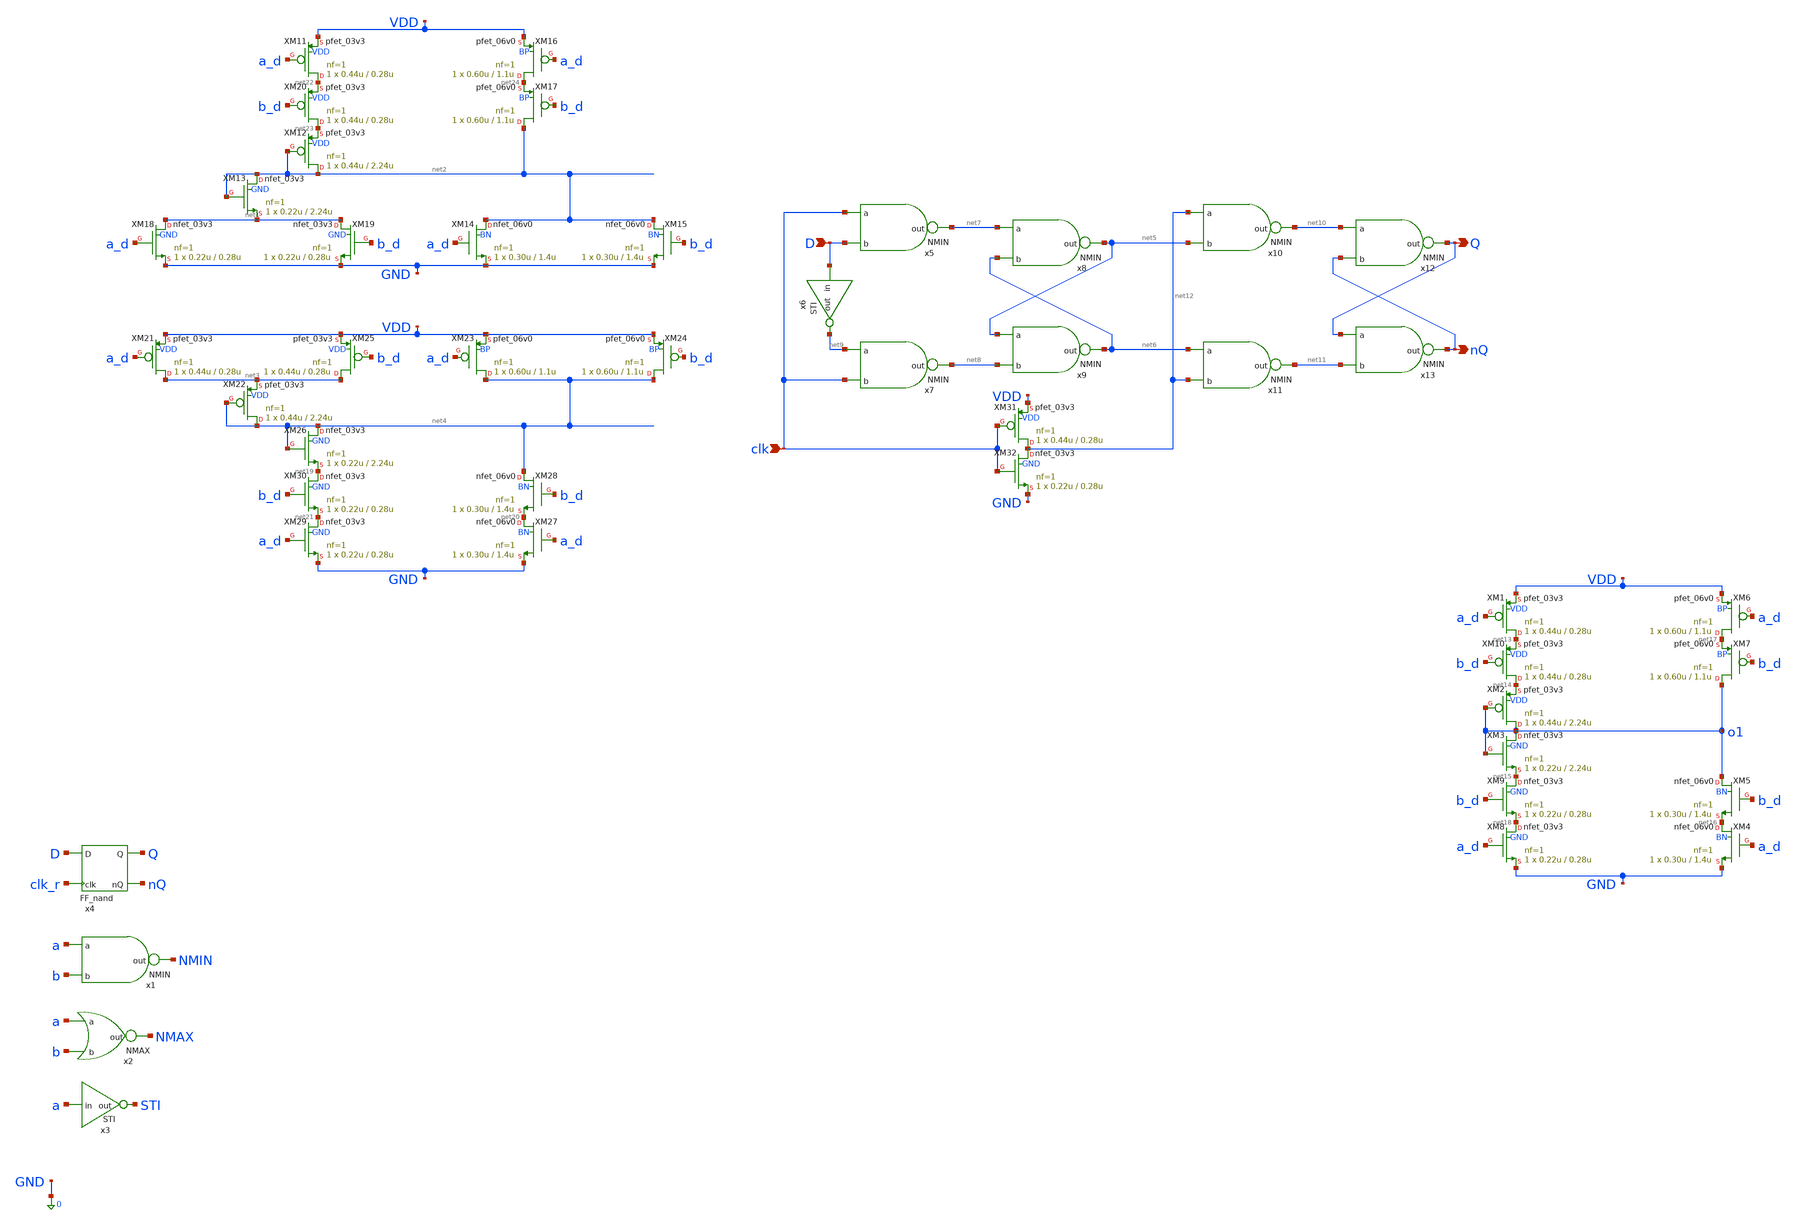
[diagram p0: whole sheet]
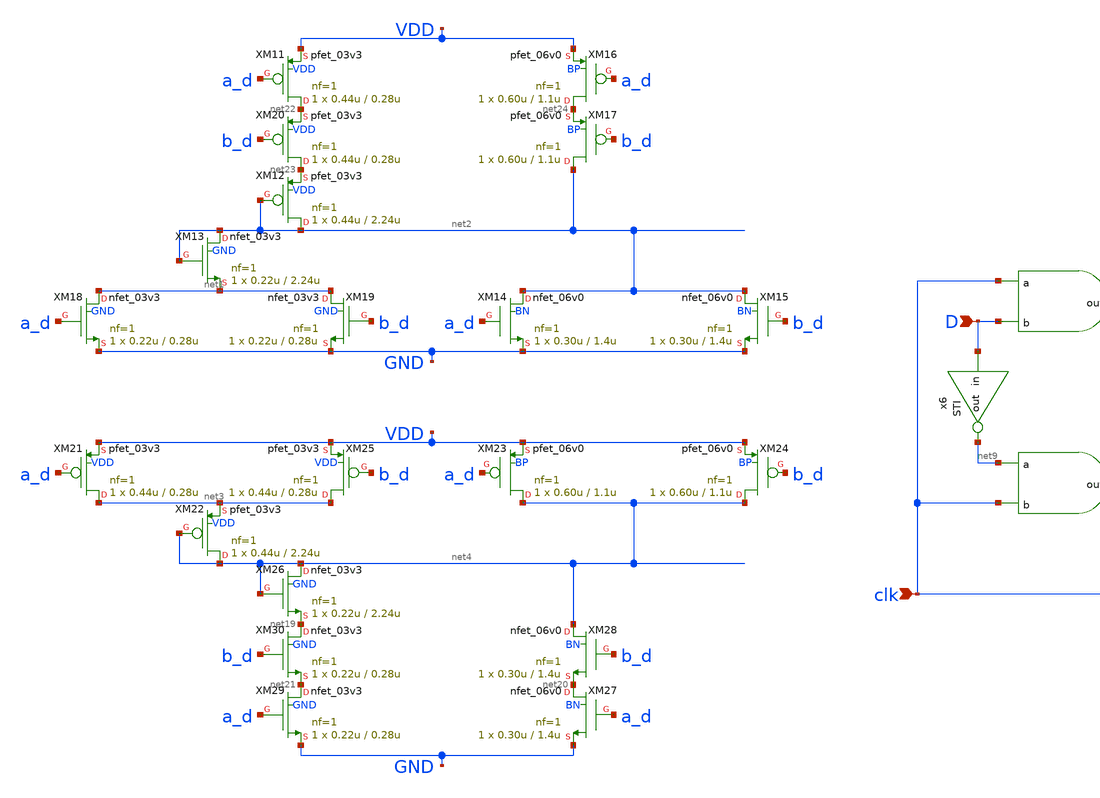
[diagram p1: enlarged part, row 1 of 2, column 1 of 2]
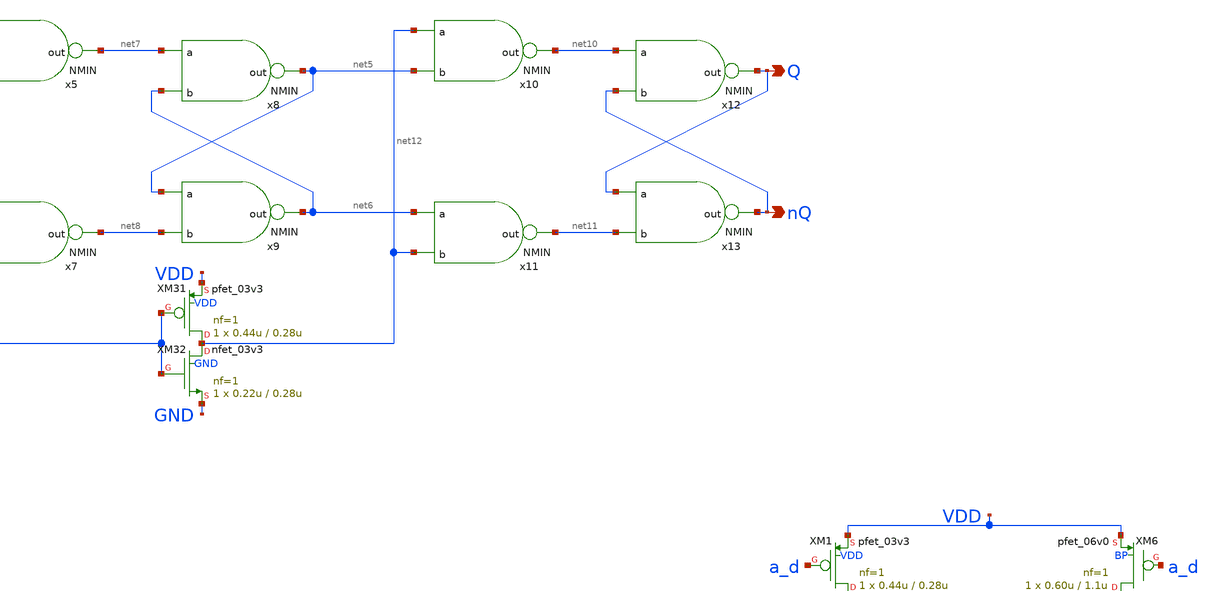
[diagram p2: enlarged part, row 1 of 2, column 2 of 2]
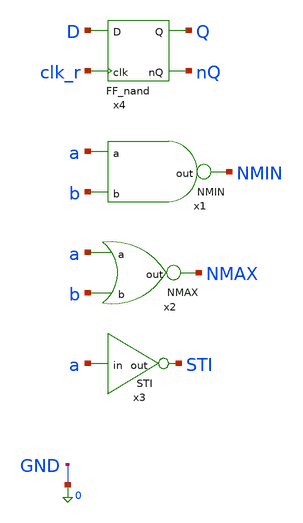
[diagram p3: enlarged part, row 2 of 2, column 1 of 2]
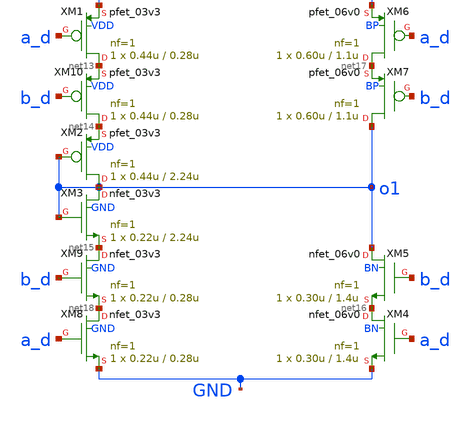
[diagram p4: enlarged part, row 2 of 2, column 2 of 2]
** sch_path: xschem_designs/NMIN_TB.sch
**.subckt NMIN_TB D clk Q nQ
*.ipin D
*.ipin clk
*.opin Q
*.opin nQ
x1 NMIN a b NMIN
XM1 net13 a_d VDD VDD pfet_03v3 L=0.28u W=0.44u nf=1 ad='int((nf+1)/2) * W/nf * 0.18u' as='int((nf+2)/2) * W/nf * 0.18u'
+ pd='2*int((nf+1)/2) * (W/nf + 0.18u)' ps='2*int((nf+2)/2) * (W/nf + 0.18u)' nrd='0.18u / W' nrs='0.18u / W'
+ sa=0 sb=0 sd=0 m=1 par=1
XM2 o1 o1 net14 VDD pfet_03v3 L=2.24u W=0.44u nf=1 ad='int((nf+1)/2) * W/nf * 0.18u' as='int((nf+2)/2) * W/nf * 0.18u'
+ pd='2*int((nf+1)/2) * (W/nf + 0.18u)' ps='2*int((nf+2)/2) * (W/nf + 0.18u)' nrd='0.18u / W' nrs='0.18u / W'
+ sa=0 sb=0 sd=0 m=1 par=1
XM3 o1 o1 net15 GND nfet_03v3 L=2.24u W=0.22u nf=1 ad='int((nf+1)/2) * W/nf * 0.18u' as='int((nf+2)/2) * W/nf * 0.18u'
+ pd='2*int((nf+1)/2) * (W/nf + 0.18u)' ps='2*int((nf+2)/2) * (W/nf + 0.18u)' nrd='0.18u / W' nrs='0.18u / W'
+ sa=0 sb=0 sd=0 m=1 par=1
XM4 net16 a_d GND BN nfet_06v0 L=1.4u W=0.30u nf=1 ad='int((nf+1)/2) * W/nf * 0.18u' as='int((nf+2)/2) * W/nf * 0.18u'
+ pd='2*int((nf+1)/2) * (W/nf + 0.18u)' ps='2*int((nf+2)/2) * (W/nf + 0.18u)' nrd='0.18u / W' nrs='0.18u / W'
+ sa=0 sb=0 sd=0 m=1 par=1
XM5 o1 b_d net16 BN nfet_06v0 L=1.4u W=0.30u nf=1 ad='int((nf+1)/2) * W/nf * 0.18u' as='int((nf+2)/2) * W/nf * 0.18u'
+ pd='2*int((nf+1)/2) * (W/nf + 0.18u)' ps='2*int((nf+2)/2) * (W/nf + 0.18u)' nrd='0.18u / W' nrs='0.18u / W'
+ sa=0 sb=0 sd=0 m=1 par=1
XM6 net17 a_d VDD BP pfet_06v0 L=1.1u W=0.60u nf=1 ad='int((nf+1)/2) * W/nf * 0.18u' as='int((nf+2)/2) * W/nf * 0.18u'
+ pd='2*int((nf+1)/2) * (W/nf + 0.18u)' ps='2*int((nf+2)/2) * (W/nf + 0.18u)' nrd='0.18u / W' nrs='0.18u / W'
+ sa=0 sb=0 sd=0 m=1 par=1
XM7 o1 b_d net17 BP pfet_06v0 L=1.1u W=0.60u nf=1 ad='int((nf+1)/2) * W/nf * 0.18u' as='int((nf+2)/2) * W/nf * 0.18u'
+ pd='2*int((nf+1)/2) * (W/nf + 0.18u)' ps='2*int((nf+2)/2) * (W/nf + 0.18u)' nrd='0.18u / W' nrs='0.18u / W'
+ sa=0 sb=0 sd=0 m=1 par=1
XM8 net18 a_d GND GND nfet_03v3 L=0.28u W=0.22u nf=1 ad='int((nf+1)/2) * W/nf * 0.18u' as='int((nf+2)/2) * W/nf * 0.18u'
+ pd='2*int((nf+1)/2) * (W/nf + 0.18u)' ps='2*int((nf+2)/2) * (W/nf + 0.18u)' nrd='0.18u / W' nrs='0.18u / W'
+ sa=0 sb=0 sd=0 m=1 par=1
XM9 net15 b_d net18 GND nfet_03v3 L=0.28u W=0.22u nf=1 ad='int((nf+1)/2) * W/nf * 0.18u' as='int((nf+2)/2) * W/nf * 0.18u'
+ pd='2*int((nf+1)/2) * (W/nf + 0.18u)' ps='2*int((nf+2)/2) * (W/nf + 0.18u)' nrd='0.18u / W' nrs='0.18u / W'
+ sa=0 sb=0 sd=0 m=1 par=1
XM10 net14 b_d net13 VDD pfet_03v3 L=0.28u W=0.44u nf=1 ad='int((nf+1)/2) * W/nf * 0.18u' as='int((nf+2)/2) * W/nf * 0.18u'
+ pd='2*int((nf+1)/2) * (W/nf + 0.18u)' ps='2*int((nf+2)/2) * (W/nf + 0.18u)' nrd='0.18u / W' nrs='0.18u / W'
+ sa=0 sb=0 sd=0 m=1 par=1
XM13 net2 net2 net1 GND nfet_03v3 L=2.24u W=0.22u nf=1 ad='int((nf+1)/2) * W/nf * 0.18u' as='int((nf+2)/2) * W/nf * 0.18u'
+ pd='2*int((nf+1)/2) * (W/nf + 0.18u)' ps='2*int((nf+2)/2) * (W/nf + 0.18u)' nrd='0.18u / W' nrs='0.18u / W'
+ sa=0 sb=0 sd=0 m=1 par=1
XM14 net2 a_d GND BN nfet_06v0 L=1.4u W=0.30u nf=1 ad='int((nf+1)/2) * W/nf * 0.18u' as='int((nf+2)/2) * W/nf * 0.18u'
+ pd='2*int((nf+1)/2) * (W/nf + 0.18u)' ps='2*int((nf+2)/2) * (W/nf + 0.18u)' nrd='0.18u / W' nrs='0.18u / W'
+ sa=0 sb=0 sd=0 m=1 par=1
XM15 net2 b_d GND BN nfet_06v0 L=1.4u W=0.30u nf=1 ad='int((nf+1)/2) * W/nf * 0.18u' as='int((nf+2)/2) * W/nf * 0.18u'
+ pd='2*int((nf+1)/2) * (W/nf + 0.18u)' ps='2*int((nf+2)/2) * (W/nf + 0.18u)' nrd='0.18u / W' nrs='0.18u / W'
+ sa=0 sb=0 sd=0 m=1 par=1
XM18 net1 a_d GND GND nfet_03v3 L=0.28u W=0.22u nf=1 ad='int((nf+1)/2) * W/nf * 0.18u' as='int((nf+2)/2) * W/nf * 0.18u'
+ pd='2*int((nf+1)/2) * (W/nf + 0.18u)' ps='2*int((nf+2)/2) * (W/nf + 0.18u)' nrd='0.18u / W' nrs='0.18u / W'
+ sa=0 sb=0 sd=0 m=1 par=1
XM19 net1 b_d GND GND nfet_03v3 L=0.28u W=0.22u nf=1 ad='int((nf+1)/2) * W/nf * 0.18u' as='int((nf+2)/2) * W/nf * 0.18u'
+ pd='2*int((nf+1)/2) * (W/nf + 0.18u)' ps='2*int((nf+2)/2) * (W/nf + 0.18u)' nrd='0.18u / W' nrs='0.18u / W'
+ sa=0 sb=0 sd=0 m=1 par=1
XM21 net3 a_d VDD VDD pfet_03v3 L=0.28u W=0.44u nf=1 ad='int((nf+1)/2) * W/nf * 0.18u' as='int((nf+2)/2) * W/nf * 0.18u'
+ pd='2*int((nf+1)/2) * (W/nf + 0.18u)' ps='2*int((nf+2)/2) * (W/nf + 0.18u)' nrd='0.18u / W' nrs='0.18u / W'
+ sa=0 sb=0 sd=0 m=1 par=1
XM22 net4 net4 net3 VDD pfet_03v3 L=2.24u W=0.44u nf=1 ad='int((nf+1)/2) * W/nf * 0.18u' as='int((nf+2)/2) * W/nf * 0.18u'
+ pd='2*int((nf+1)/2) * (W/nf + 0.18u)' ps='2*int((nf+2)/2) * (W/nf + 0.18u)' nrd='0.18u / W' nrs='0.18u / W'
+ sa=0 sb=0 sd=0 m=1 par=1
XM23 net4 a_d VDD BP pfet_06v0 L=1.1u W=0.60u nf=1 ad='int((nf+1)/2) * W/nf * 0.18u' as='int((nf+2)/2) * W/nf * 0.18u'
+ pd='2*int((nf+1)/2) * (W/nf + 0.18u)' ps='2*int((nf+2)/2) * (W/nf + 0.18u)' nrd='0.18u / W' nrs='0.18u / W'
+ sa=0 sb=0 sd=0 m=1 par=1
XM24 net4 b_d VDD BP pfet_06v0 L=1.1u W=0.60u nf=1 ad='int((nf+1)/2) * W/nf * 0.18u' as='int((nf+2)/2) * W/nf * 0.18u'
+ pd='2*int((nf+1)/2) * (W/nf + 0.18u)' ps='2*int((nf+2)/2) * (W/nf + 0.18u)' nrd='0.18u / W' nrs='0.18u / W'
+ sa=0 sb=0 sd=0 m=1 par=1
XM25 net3 b_d VDD VDD pfet_03v3 L=0.28u W=0.44u nf=1 ad='int((nf+1)/2) * W/nf * 0.18u' as='int((nf+2)/2) * W/nf * 0.18u'
+ pd='2*int((nf+1)/2) * (W/nf + 0.18u)' ps='2*int((nf+2)/2) * (W/nf + 0.18u)' nrd='0.18u / W' nrs='0.18u / W'
+ sa=0 sb=0 sd=0 m=1 par=1
XM26 net4 net4 net19 GND nfet_03v3 L=2.24u W=0.22u nf=1 ad='int((nf+1)/2) * W/nf * 0.18u' as='int((nf+2)/2) * W/nf * 0.18u'
+ pd='2*int((nf+1)/2) * (W/nf + 0.18u)' ps='2*int((nf+2)/2) * (W/nf + 0.18u)' nrd='0.18u / W' nrs='0.18u / W'
+ sa=0 sb=0 sd=0 m=1 par=1
XM27 net20 a_d GND BN nfet_06v0 L=1.4u W=0.30u nf=1 ad='int((nf+1)/2) * W/nf * 0.18u' as='int((nf+2)/2) * W/nf * 0.18u'
+ pd='2*int((nf+1)/2) * (W/nf + 0.18u)' ps='2*int((nf+2)/2) * (W/nf + 0.18u)' nrd='0.18u / W' nrs='0.18u / W'
+ sa=0 sb=0 sd=0 m=1 par=1
XM28 net4 b_d net20 BN nfet_06v0 L=1.4u W=0.30u nf=1 ad='int((nf+1)/2) * W/nf * 0.18u' as='int((nf+2)/2) * W/nf * 0.18u'
+ pd='2*int((nf+1)/2) * (W/nf + 0.18u)' ps='2*int((nf+2)/2) * (W/nf + 0.18u)' nrd='0.18u / W' nrs='0.18u / W'
+ sa=0 sb=0 sd=0 m=1 par=1
XM29 net21 a_d GND GND nfet_03v3 L=0.28u W=0.22u nf=1 ad='int((nf+1)/2) * W/nf * 0.18u' as='int((nf+2)/2) * W/nf * 0.18u'
+ pd='2*int((nf+1)/2) * (W/nf + 0.18u)' ps='2*int((nf+2)/2) * (W/nf + 0.18u)' nrd='0.18u / W' nrs='0.18u / W'
+ sa=0 sb=0 sd=0 m=1 par=1
XM30 net19 b_d net21 GND nfet_03v3 L=0.28u W=0.22u nf=1 ad='int((nf+1)/2) * W/nf * 0.18u' as='int((nf+2)/2) * W/nf * 0.18u'
+ pd='2*int((nf+1)/2) * (W/nf + 0.18u)' ps='2*int((nf+2)/2) * (W/nf + 0.18u)' nrd='0.18u / W' nrs='0.18u / W'
+ sa=0 sb=0 sd=0 m=1 par=1
XM11 net22 a_d VDD VDD pfet_03v3 L=0.28u W=0.44u nf=1 ad='int((nf+1)/2) * W/nf * 0.18u' as='int((nf+2)/2) * W/nf * 0.18u'
+ pd='2*int((nf+1)/2) * (W/nf + 0.18u)' ps='2*int((nf+2)/2) * (W/nf + 0.18u)' nrd='0.18u / W' nrs='0.18u / W'
+ sa=0 sb=0 sd=0 m=1 par=1
XM12 net2 net2 net23 VDD pfet_03v3 L=2.24u W=0.44u nf=1 ad='int((nf+1)/2) * W/nf * 0.18u' as='int((nf+2)/2) * W/nf * 0.18u'
+ pd='2*int((nf+1)/2) * (W/nf + 0.18u)' ps='2*int((nf+2)/2) * (W/nf + 0.18u)' nrd='0.18u / W' nrs='0.18u / W'
+ sa=0 sb=0 sd=0 m=1 par=1
XM16 net24 a_d VDD BP pfet_06v0 L=1.1u W=0.60u nf=1 ad='int((nf+1)/2) * W/nf * 0.18u' as='int((nf+2)/2) * W/nf * 0.18u'
+ pd='2*int((nf+1)/2) * (W/nf + 0.18u)' ps='2*int((nf+2)/2) * (W/nf + 0.18u)' nrd='0.18u / W' nrs='0.18u / W'
+ sa=0 sb=0 sd=0 m=1 par=1
XM17 net2 b_d net24 BP pfet_06v0 L=1.1u W=0.60u nf=1 ad='int((nf+1)/2) * W/nf * 0.18u' as='int((nf+2)/2) * W/nf * 0.18u'
+ pd='2*int((nf+1)/2) * (W/nf + 0.18u)' ps='2*int((nf+2)/2) * (W/nf + 0.18u)' nrd='0.18u / W' nrs='0.18u / W'
+ sa=0 sb=0 sd=0 m=1 par=1
XM20 net23 b_d net22 VDD pfet_03v3 L=0.28u W=0.44u nf=1 ad='int((nf+1)/2) * W/nf * 0.18u' as='int((nf+2)/2) * W/nf * 0.18u'
+ pd='2*int((nf+1)/2) * (W/nf + 0.18u)' ps='2*int((nf+2)/2) * (W/nf + 0.18u)' nrd='0.18u / W' nrs='0.18u / W'
+ sa=0 sb=0 sd=0 m=1 par=1
x2 NMAX a b NMAX
x3 a STI STI
x4 D Q nQ clk_r FF_nand
x5 net7 clk D NMIN
x6 D net9 STI
x7 net8 net9 clk NMIN
x8 net5 net7 net6 NMIN
x9 net6 net5 net8 NMIN
x10 net10 net12 net5 NMIN
x11 net11 net6 net12 NMIN
x12 Q net10 nQ NMIN
x13 nQ Q net11 NMIN
XM31 net12 clk VDD VDD pfet_03v3 L=0.28u W=0.44u nf=1 ad='int((nf+1)/2) * W/nf * 0.18u' as='int((nf+2)/2) * W/nf * 0.18u'
+ pd='2*int((nf+1)/2) * (W/nf + 0.18u)' ps='2*int((nf+2)/2) * (W/nf + 0.18u)' nrd='0.18u / W' nrs='0.18u / W'
+ sa=0 sb=0 sd=0 m=1 par=1
XM32 net12 clk GND GND nfet_03v3 L=0.28u W=0.22u nf=1 ad='int((nf+1)/2) * W/nf * 0.18u' as='int((nf+2)/2) * W/nf * 0.18u'
+ pd='2*int((nf+1)/2) * (W/nf + 0.18u)' ps='2*int((nf+2)/2) * (W/nf + 0.18u)' nrd='0.18u / W' nrs='0.18u / W'
+ sa=0 sb=0 sd=0 m=1 par=1
**** begin user architecture code


.global VDD GND BP BN
.option temp=27
.include /usr/local/share/pdk/gf180mcuC/libs.tech/ngspice/design.ngspice
.lib /usr/local/share/pdk/gf180mcuC/libs.tech/ngspice/sm141064.ngspice typical

Vdd VDD 0 3.3
Vbp BP VDD 2.7
Vbn BN GND -2.7
Va a 0 PWL(0 0 89.9n 0 90.1n 1.4 179.9n 1.4 180.1n 3.3 270n 3.3)
Vb b 0 PWL(0 0 29.9n 0 30.1n 1.4 59.9n 1.4 60.1n 3.3 89.9n 3.3 90.1n 0 119.9n 0 120.1n 1.4 149.9n
+ 1.4 150.1n 3.3 179.9n 3.3 180.1n 0 209.9n 0 210.1n 1.4 239.9n 1.4 240.1n 3.3 270n 3.3)
VD D 0 PWL(0n 0 14.9n 0 15.1n 1.4 74.9n 1.4 75.1n 3.3 134.9n 3.3 135.1n 1.4 194.9n 1.4 195.1n 0
+ 254.9n 0 255.1n 3.3 314.9n 3.3 315.1n 0 374.9n 0 375.1n 0 434.9ns 0 435.1n 1.4 494.9n 1.4 495.1n 1.4
+ 554.9n 1.4 555.1n 3.3 615n 3.3)
Vclk_r clk_r 0 PULSE(0 3.3 29.9n 0.2n 0.2n 29.8n 60n)
Vclk_f clk_f 0 PULSE(3.3 0 29.9n 0.2n 0.2n 29.8n 60n)

.control
  save all
  tran 0.05n 550n
  write NMIN_TB.raw
.endc
.end


**** end user architecture code
**.ends

* expanding   symbol:  xschem_designs/NMIN.sym # of pins=3
** sym_path: xschem_designs/NMIN.sym
** sch_path: xschem_designs/NMIN.sch
.subckt NMIN out a b
*.ipin a
*.ipin b
*.opin out
XM21 net1 a VDD VDD pfet_03v3 L=0.28u W=0.44u nf=1 ad='int((nf+1)/2) * W/nf * 0.18u' as='int((nf+2)/2) * W/nf * 0.18u'
+ pd='2*int((nf+1)/2) * (W/nf + 0.18u)' ps='2*int((nf+2)/2) * (W/nf + 0.18u)' nrd='0.18u / W' nrs='0.18u / W'
+ sa=0 sb=0 sd=0 m=1 par=1
XM22 out out net1 VDD pfet_03v3 L=2.24u W=0.44u nf=1 ad='int((nf+1)/2) * W/nf * 0.18u' as='int((nf+2)/2) * W/nf * 0.18u'
+ pd='2*int((nf+1)/2) * (W/nf + 0.18u)' ps='2*int((nf+2)/2) * (W/nf + 0.18u)' nrd='0.18u / W' nrs='0.18u / W'
+ sa=0 sb=0 sd=0 m=1 par=1
XM23 out a VDD BP pfet_06v0 L=1.1u W=0.60u nf=1 ad='int((nf+1)/2) * W/nf * 0.18u' as='int((nf+2)/2) * W/nf * 0.18u'
+ pd='2*int((nf+1)/2) * (W/nf + 0.18u)' ps='2*int((nf+2)/2) * (W/nf + 0.18u)' nrd='0.18u / W' nrs='0.18u / W'
+ sa=0 sb=0 sd=0 m=1 par=1
XM24 out b VDD BP pfet_06v0 L=1.1u W=0.60u nf=1 ad='int((nf+1)/2) * W/nf * 0.18u' as='int((nf+2)/2) * W/nf * 0.18u'
+ pd='2*int((nf+1)/2) * (W/nf + 0.18u)' ps='2*int((nf+2)/2) * (W/nf + 0.18u)' nrd='0.18u / W' nrs='0.18u / W'
+ sa=0 sb=0 sd=0 m=1 par=1
XM25 net1 b VDD VDD pfet_03v3 L=0.28u W=0.44u nf=1 ad='int((nf+1)/2) * W/nf * 0.18u' as='int((nf+2)/2) * W/nf * 0.18u'
+ pd='2*int((nf+1)/2) * (W/nf + 0.18u)' ps='2*int((nf+2)/2) * (W/nf + 0.18u)' nrd='0.18u / W' nrs='0.18u / W'
+ sa=0 sb=0 sd=0 m=1 par=1
XM26 out out net2 GND nfet_03v3 L=2.24u W=0.22u nf=1 ad='int((nf+1)/2) * W/nf * 0.18u' as='int((nf+2)/2) * W/nf * 0.18u'
+ pd='2*int((nf+1)/2) * (W/nf + 0.18u)' ps='2*int((nf+2)/2) * (W/nf + 0.18u)' nrd='0.18u / W' nrs='0.18u / W'
+ sa=0 sb=0 sd=0 m=1 par=1
XM27 net3 a GND BN nfet_06v0 L=1.4u W=0.30u nf=1 ad='int((nf+1)/2) * W/nf * 0.18u' as='int((nf+2)/2) * W/nf * 0.18u'
+ pd='2*int((nf+1)/2) * (W/nf + 0.18u)' ps='2*int((nf+2)/2) * (W/nf + 0.18u)' nrd='0.18u / W' nrs='0.18u / W'
+ sa=0 sb=0 sd=0 m=1 par=1
XM28 out b net3 BN nfet_06v0 L=1.4u W=0.30u nf=1 ad='int((nf+1)/2) * W/nf * 0.18u' as='int((nf+2)/2) * W/nf * 0.18u'
+ pd='2*int((nf+1)/2) * (W/nf + 0.18u)' ps='2*int((nf+2)/2) * (W/nf + 0.18u)' nrd='0.18u / W' nrs='0.18u / W'
+ sa=0 sb=0 sd=0 m=1 par=1
XM29 net4 a GND GND nfet_03v3 L=0.28u W=0.22u nf=1 ad='int((nf+1)/2) * W/nf * 0.18u' as='int((nf+2)/2) * W/nf * 0.18u'
+ pd='2*int((nf+1)/2) * (W/nf + 0.18u)' ps='2*int((nf+2)/2) * (W/nf + 0.18u)' nrd='0.18u / W' nrs='0.18u / W'
+ sa=0 sb=0 sd=0 m=1 par=1
XM30 net2 b net4 GND nfet_03v3 L=0.28u W=0.22u nf=1 ad='int((nf+1)/2) * W/nf * 0.18u' as='int((nf+2)/2) * W/nf * 0.18u'
+ pd='2*int((nf+1)/2) * (W/nf + 0.18u)' ps='2*int((nf+2)/2) * (W/nf + 0.18u)' nrd='0.18u / W' nrs='0.18u / W'
+ sa=0 sb=0 sd=0 m=1 par=1
.ends


* expanding   symbol:  xschem_designs/NMAX.sym # of pins=3
** sym_path: xschem_designs/NMAX.sym
** sch_path: xschem_designs/NMAX.sch
.subckt NMAX out a b
*.ipin a
*.ipin b
*.opin out
XM13 out out net1 GND nfet_03v3 L=2.24u W=0.22u nf=1 ad='int((nf+1)/2) * W/nf * 0.18u' as='int((nf+2)/2) * W/nf * 0.18u'
+ pd='2*int((nf+1)/2) * (W/nf + 0.18u)' ps='2*int((nf+2)/2) * (W/nf + 0.18u)' nrd='0.18u / W' nrs='0.18u / W'
+ sa=0 sb=0 sd=0 m=1 par=1
XM14 out a GND BN nfet_06v0 L=1.4u W=0.30u nf=1 ad='int((nf+1)/2) * W/nf * 0.18u' as='int((nf+2)/2) * W/nf * 0.18u'
+ pd='2*int((nf+1)/2) * (W/nf + 0.18u)' ps='2*int((nf+2)/2) * (W/nf + 0.18u)' nrd='0.18u / W' nrs='0.18u / W'
+ sa=0 sb=0 sd=0 m=1 par=1
XM15 out b GND BN nfet_06v0 L=1.4u W=0.30u nf=1 ad='int((nf+1)/2) * W/nf * 0.18u' as='int((nf+2)/2) * W/nf * 0.18u'
+ pd='2*int((nf+1)/2) * (W/nf + 0.18u)' ps='2*int((nf+2)/2) * (W/nf + 0.18u)' nrd='0.18u / W' nrs='0.18u / W'
+ sa=0 sb=0 sd=0 m=1 par=1
XM18 net1 a GND GND nfet_03v3 L=0.28u W=0.22u nf=1 ad='int((nf+1)/2) * W/nf * 0.18u' as='int((nf+2)/2) * W/nf * 0.18u'
+ pd='2*int((nf+1)/2) * (W/nf + 0.18u)' ps='2*int((nf+2)/2) * (W/nf + 0.18u)' nrd='0.18u / W' nrs='0.18u / W'
+ sa=0 sb=0 sd=0 m=1 par=1
XM19 net1 b GND GND nfet_03v3 L=0.28u W=0.22u nf=1 ad='int((nf+1)/2) * W/nf * 0.18u' as='int((nf+2)/2) * W/nf * 0.18u'
+ pd='2*int((nf+1)/2) * (W/nf + 0.18u)' ps='2*int((nf+2)/2) * (W/nf + 0.18u)' nrd='0.18u / W' nrs='0.18u / W'
+ sa=0 sb=0 sd=0 m=1 par=1
XM11 net2 a VDD VDD pfet_03v3 L=0.28u W=0.44u nf=1 ad='int((nf+1)/2) * W/nf * 0.18u' as='int((nf+2)/2) * W/nf * 0.18u'
+ pd='2*int((nf+1)/2) * (W/nf + 0.18u)' ps='2*int((nf+2)/2) * (W/nf + 0.18u)' nrd='0.18u / W' nrs='0.18u / W'
+ sa=0 sb=0 sd=0 m=1 par=1
XM12 out out net3 VDD pfet_03v3 L=1.12u W=0.22u nf=1 ad='int((nf+1)/2) * W/nf * 0.18u' as='int((nf+2)/2) * W/nf * 0.18u'
+ pd='2*int((nf+1)/2) * (W/nf + 0.18u)' ps='2*int((nf+2)/2) * (W/nf + 0.18u)' nrd='0.18u / W' nrs='0.18u / W'
+ sa=0 sb=0 sd=0 m=1 par=1
XM16 net4 a VDD BP pfet_06v0 L=1.1u W=0.60u nf=1 ad='int((nf+1)/2) * W/nf * 0.18u' as='int((nf+2)/2) * W/nf * 0.18u'
+ pd='2*int((nf+1)/2) * (W/nf + 0.18u)' ps='2*int((nf+2)/2) * (W/nf + 0.18u)' nrd='0.18u / W' nrs='0.18u / W'
+ sa=0 sb=0 sd=0 m=1 par=1
XM17 out b net4 BP pfet_06v0 L=1.1u W=0.60u nf=1 ad='int((nf+1)/2) * W/nf * 0.18u' as='int((nf+2)/2) * W/nf * 0.18u'
+ pd='2*int((nf+1)/2) * (W/nf + 0.18u)' ps='2*int((nf+2)/2) * (W/nf + 0.18u)' nrd='0.18u / W' nrs='0.18u / W'
+ sa=0 sb=0 sd=0 m=1 par=1
XM20 net3 b net2 VDD pfet_03v3 L=0.28u W=0.44u nf=1 ad='int((nf+1)/2) * W/nf * 0.18u' as='int((nf+2)/2) * W/nf * 0.18u'
+ pd='2*int((nf+1)/2) * (W/nf + 0.18u)' ps='2*int((nf+2)/2) * (W/nf + 0.18u)' nrd='0.18u / W' nrs='0.18u / W'
+ sa=0 sb=0 sd=0 m=1 par=1
.ends


* expanding   symbol:  xschem_designs/STI.sym # of pins=2
** sym_path: xschem_designs/STI.sym
** sch_path: xschem_designs/STI.sch
.subckt STI in out
*.ipin in
*.opin out
XM225 out out net1 GND nfet_03v3 L=2.24u W=0.22u nf=1 ad='int((nf+1)/2) * W/nf * 0.18u' as='int((nf+2)/2) * W/nf * 0.18u'
+ pd='2*int((nf+1)/2) * (W/nf + 0.18u)' ps='2*int((nf+2)/2) * (W/nf + 0.18u)' nrd='0.18u / W' nrs='0.18u / W'
+ sa=0 sb=0 sd=0 m=1 par=1
XM226 out out net2 VDD pfet_03v3 L=1.12u W=0.22u nf=1 ad='int((nf+1)/2) * W/nf * 0.18u' as='int((nf+2)/2) * W/nf * 0.18u'
+ pd='2*int((nf+1)/2) * (W/nf + 0.18u)' ps='2*int((nf+2)/2) * (W/nf + 0.18u)' nrd='0.18u / W' nrs='0.18u / W'
+ sa=0 sb=0 sd=0 m=1 par=1
XM237 net2 in VDD VDD pfet_03v3 L=0.28u W=0.44u nf=1 ad='int((nf+1)/2) * W/nf * 0.18u' as='int((nf+2)/2) * W/nf * 0.18u'
+ pd='2*int((nf+1)/2) * (W/nf + 0.18u)' ps='2*int((nf+2)/2) * (W/nf + 0.18u)' nrd='0.18u / W' nrs='0.18u / W'
+ sa=0 sb=0 sd=0 m=1 par=1
XM238 net1 in GND GND nfet_03v3 L=0.28u W=0.22u nf=1 ad='int((nf+1)/2) * W/nf * 0.18u' as='int((nf+2)/2) * W/nf * 0.18u'
+ pd='2*int((nf+1)/2) * (W/nf + 0.18u)' ps='2*int((nf+2)/2) * (W/nf + 0.18u)' nrd='0.18u / W' nrs='0.18u / W'
+ sa=0 sb=0 sd=0 m=1 par=1
XM241 out in VDD BP pfet_06v0 L=1.1u W=0.60u nf=1 ad='int((nf+1)/2) * W/nf * 0.18u' as='int((nf+2)/2) * W/nf * 0.18u'
+ pd='2*int((nf+1)/2) * (W/nf + 0.18u)' ps='2*int((nf+2)/2) * (W/nf + 0.18u)' nrd='0.18u / W' nrs='0.18u / W'
+ sa=0 sb=0 sd=0 m=1 par=1
XM242 out in GND BN nfet_06v0 L=1.4u W=0.30u nf=1 ad='int((nf+1)/2) * W/nf * 0.18u' as='int((nf+2)/2) * W/nf * 0.18u'
+ pd='2*int((nf+1)/2) * (W/nf + 0.18u)' ps='2*int((nf+2)/2) * (W/nf + 0.18u)' nrd='0.18u / W' nrs='0.18u / W'
+ sa=0 sb=0 sd=0 m=1 par=1
.ends


* expanding   symbol:  xschem_designs/FF_nand.sym # of pins=4
** sym_path: xschem_designs/FF_nand.sym
** sch_path: xschem_designs/FF_nand.sch
.subckt FF_nand D Q nQ clk
*.ipin D
*.ipin clk
*.opin Q
*.opin nQ
x1 net3 clk D NMIN
x3 D net5 STI
x4 net4 net5 clk NMIN
x5 net1 net3 net2 NMIN
x6 net2 net1 net4 NMIN
x7 net6 net8 net1 NMIN
x8 net7 net2 net8 NMIN
x9 Q net6 nQ NMIN
x10 nQ Q net7 NMIN
XM21 net8 clk VDD VDD pfet_03v3 L=0.28u W=0.44u nf=1 ad='int((nf+1)/2) * W/nf * 0.18u' as='int((nf+2)/2) * W/nf * 0.18u'
+ pd='2*int((nf+1)/2) * (W/nf + 0.18u)' ps='2*int((nf+2)/2) * (W/nf + 0.18u)' nrd='0.18u / W' nrs='0.18u / W'
+ sa=0 sb=0 sd=0 m=1 par=1
XM29 net8 clk GND GND nfet_03v3 L=0.28u W=0.22u nf=1 ad='int((nf+1)/2) * W/nf * 0.18u' as='int((nf+2)/2) * W/nf * 0.18u'
+ pd='2*int((nf+1)/2) * (W/nf + 0.18u)' ps='2*int((nf+2)/2) * (W/nf + 0.18u)' nrd='0.18u / W' nrs='0.18u / W'
+ sa=0 sb=0 sd=0 m=1 par=1
.ends

.end
